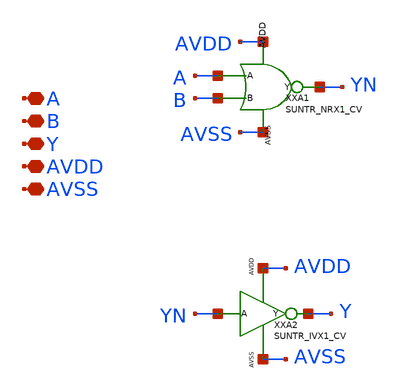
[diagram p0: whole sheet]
** sch_path: ip/sun_tr_sky130nm/design/SUN_TR_SKY130NM/SUNTR_ORX1_CV.sch
**.subckt SUNTR_ORX1_CV A B Y AVDD AVSS
*.iopin A
*.iopin B
*.iopin Y
*.iopin AVDD
*.iopin AVSS
XXA1 A B YN AVDD AVSS SUNTR_NRX1_CV
XXA2 YN Y AVDD AVSS SUNTR_IVX1_CV
**.ends
.end
